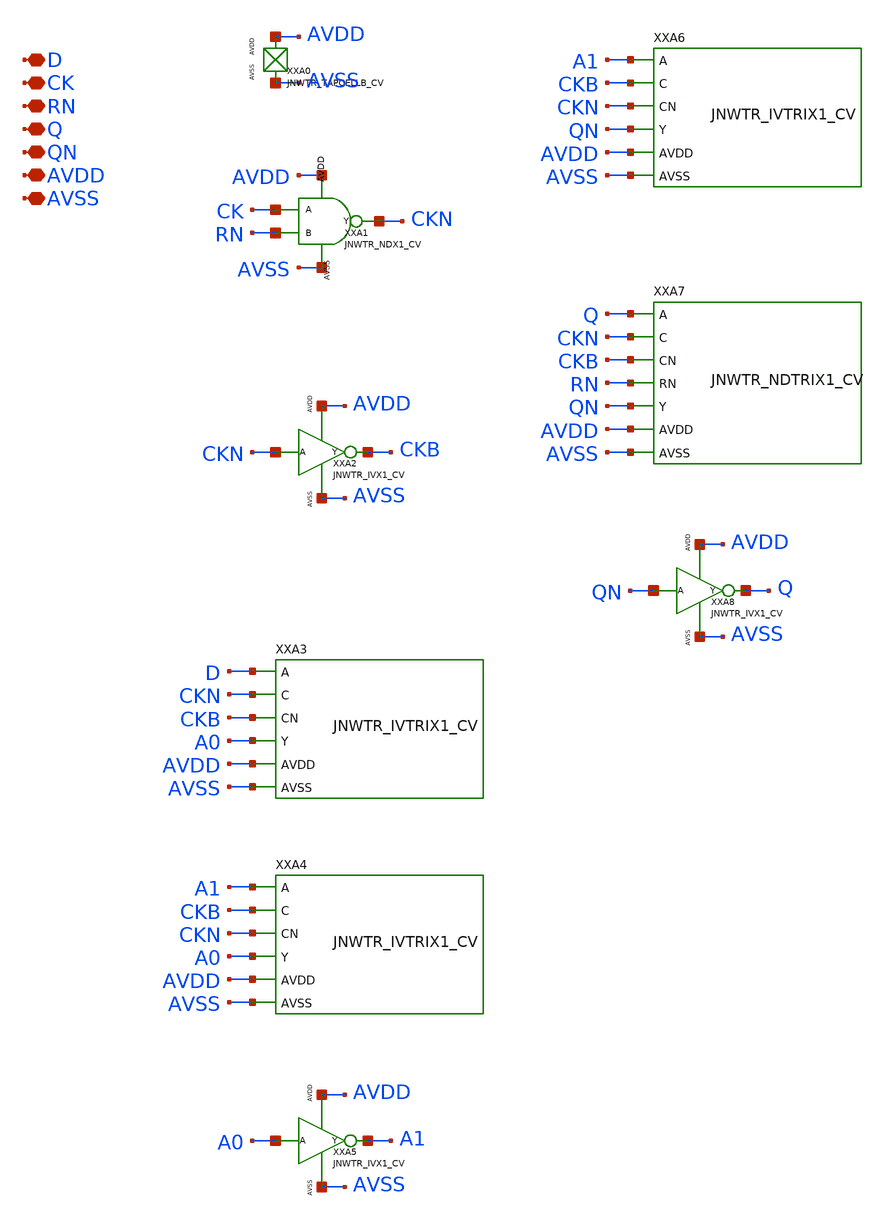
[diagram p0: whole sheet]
** sch_path: design/JNW_TR_SKY130A/JNWTR_DFRNQNX1_CV.sch
**.subckt JNWTR_DFRNQNX1_CV D CK RN Q QN AVDD AVSS
*.iopin D
*.iopin CK
*.iopin RN
*.iopin Q
*.iopin QN
*.iopin AVDD
*.iopin AVSS
XXA0 AVDD AVSS JNWTR_TAPCELLB_CV xoffset=0 yoffset=0 angle=0
XXA1 CK RN CKN AVDD AVSS JNWTR_NDX1_CV
XXA2 CKN CKB AVDD AVSS JNWTR_IVX1_CV
XXA3 D CKN CKB A0 AVDD AVSS JNWTR_IVTRIX1_CV xoffset=0 yoffset=0 angle=0
XXA4 A1 CKB CKN A0 AVDD AVSS JNWTR_IVTRIX1_CV xoffset=0 yoffset=0 angle=0
XXA5 A0 A1 AVDD AVSS JNWTR_IVX1_CV
XXA6 A1 CKB CKN QN AVDD AVSS JNWTR_IVTRIX1_CV xoffset=0 yoffset=0 angle=0
XXA7 Q CKN CKB RN QN AVDD AVSS JNWTR_NDTRIX1_CV xoffset=0 yoffset=0 angle=0
XXA8 QN Q AVDD AVSS JNWTR_IVX1_CV
**.ends
.end
